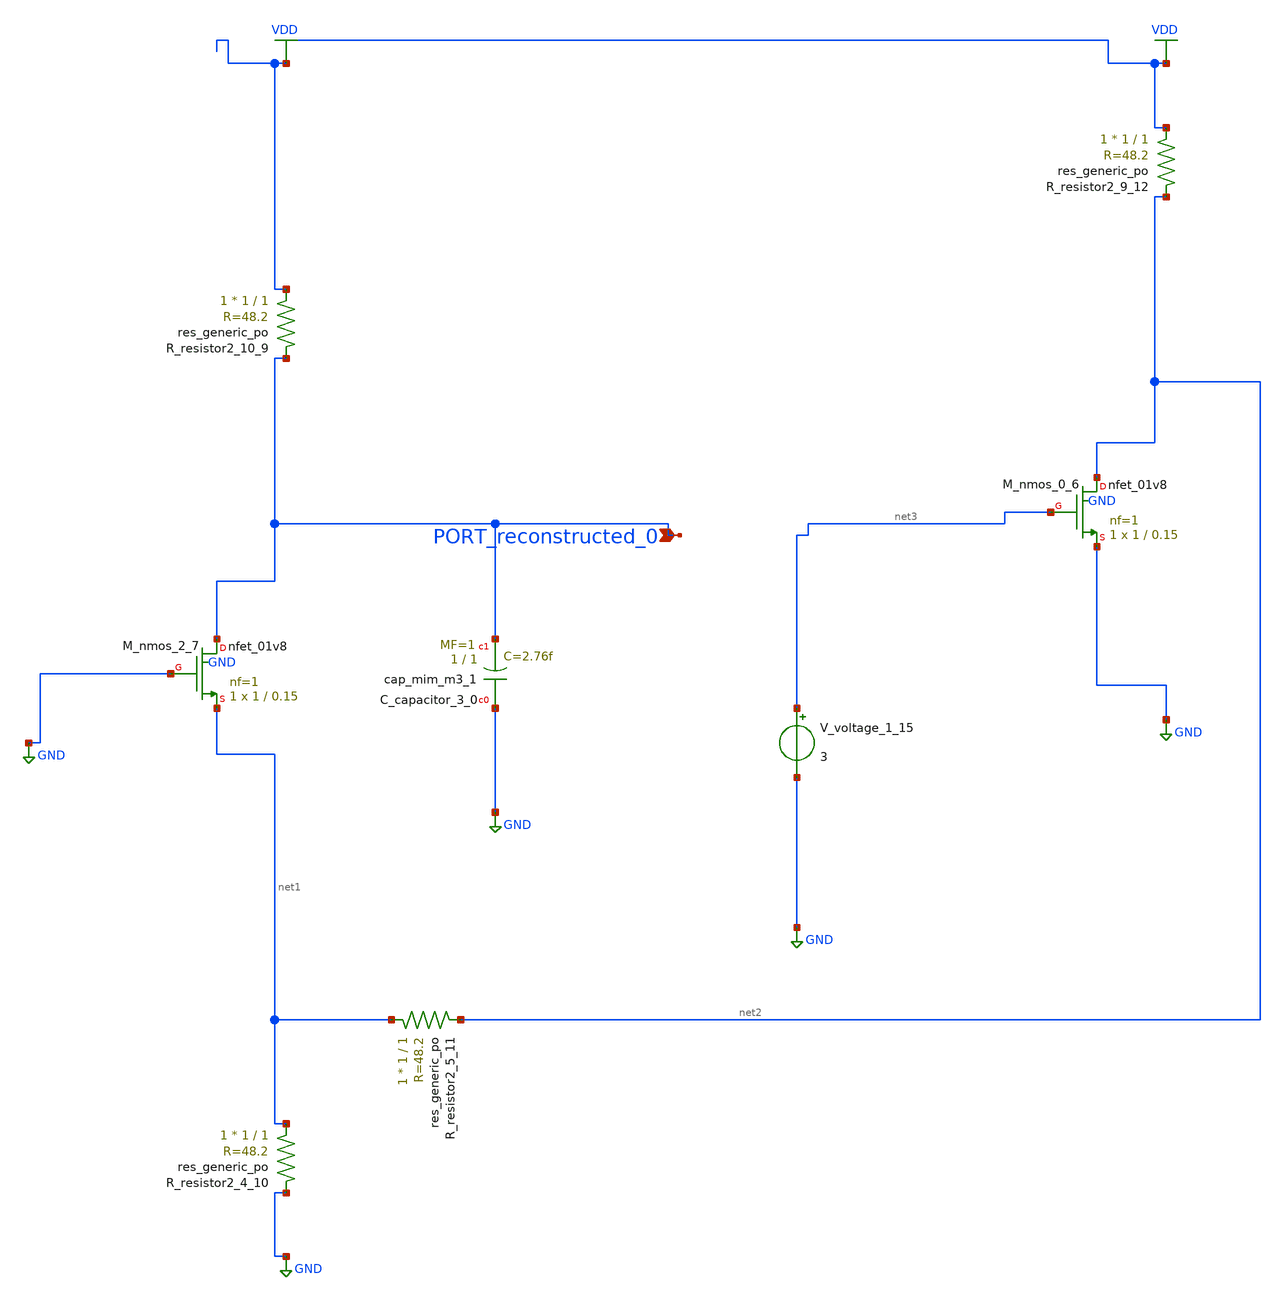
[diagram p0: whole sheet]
** sch_path: schematics/AMSNet/599.sch
**.subckt 599 PORT_reconstructed_0
*.ipin PORT_reconstructed_0
XC_capacitor_3_0 GND PORT_reconstructed_0 sky130_fd_pr__cap_mim_m3_1 W=1 L=1 MF=1 m=1
XM_nmos_0_6 net2 net3 GND GND sky130_fd_pr__nfet_01v8 L=0.15 W=1 nf=1 ad='int((1 + 1)/2) * 1 / 1 * 0.29'
+ as='int((1 + 2)/2) * 1 / 1 * 0.29' pd='2*int((1 + 1)/2) * (1 / 1 + 0.29)' ps='2*int((1 + 2)/2) * (1 / 1 + 0.29)'
+ nrd='0.29 / 1 ' nrs='0.29 / 1 ' sa=0 sb=0 sd=0 mult=1 m=1
XM_nmos_2_7 PORT_reconstructed_0 GND net1 GND sky130_fd_pr__nfet_01v8 L=0.15 W=1 nf=1 ad='int((1 + 1)/2) * 1 / 1 * 0.29'
+ as='int((1 + 2)/2) * 1 / 1 * 0.29' pd='2*int((1 + 1)/2) * (1 / 1 + 0.29)' ps='2*int((1 + 2)/2) * (1 / 1 + 0.29)'
+ nrd='0.29 / 1 ' nrs='0.29 / 1 ' sa=0 sb=0 sd=0 mult=1 m=1
XR_resistor2_10_9 VDD PORT_reconstructed_0 sky130_fd_pr__res_generic_po W=1 L=1 m=1
XR_resistor2_4_10 net1 GND sky130_fd_pr__res_generic_po W=1 L=1 m=1
XR_resistor2_5_11 net1 net2 sky130_fd_pr__res_generic_po W=1 L=1 m=1
XR_resistor2_9_12 VDD net2 sky130_fd_pr__res_generic_po W=1 L=1 m=1
V_voltage_1_15 net3 GND 3
**.ends
.GLOBAL GND
.GLOBAL VDD
.end
